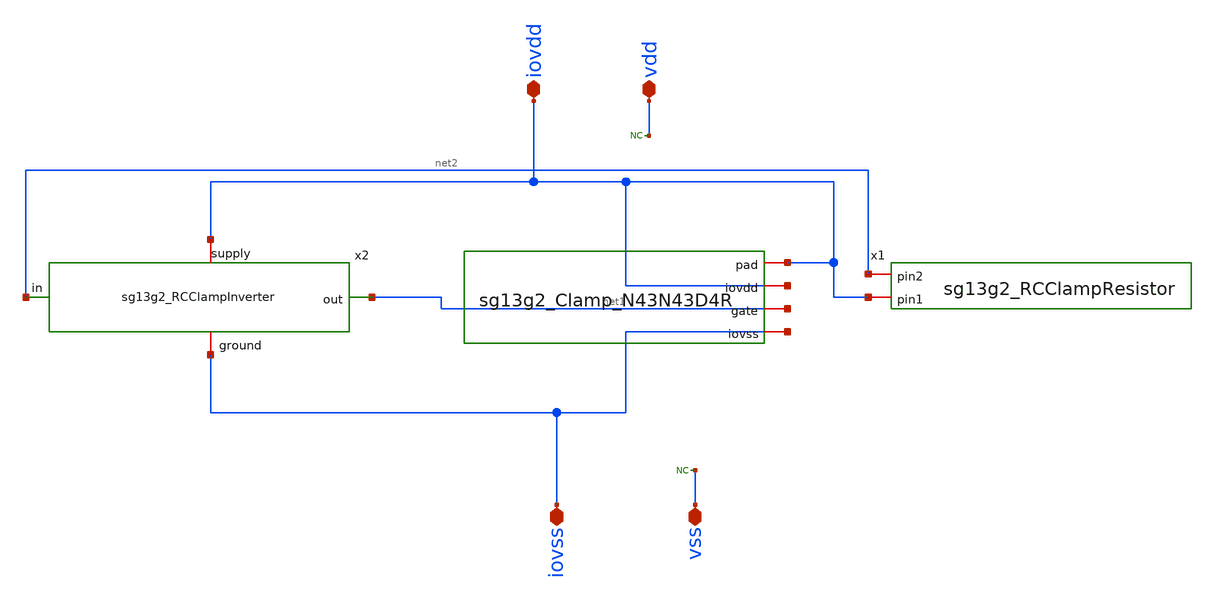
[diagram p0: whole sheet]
** sch_path: OTA_Telescopic_NO_FLATTEN/Schematics_and_Symbols/IOCells/sg13g2_IOPadIOVdd.sch
**.subckt sg13g2_IOPadIOVdd iovss iovdd vss vdd
*.iopin iovss
*.iopin iovdd
*.iopin vss
*.iopin vdd
x1 iovdd iovdd net1 iovss sg13g2_Clamp_N43N43D4R
x1 net2 iovdd sg13g2_RCClampResistor
x2 iovdd net1 net2 iovss sg13g2_RCClampInverter
* noconn vss
* noconn vdd
**.ends

* expanding   symbol:  sg13g2_Clamp_N43N43D4R.sym # of pins=4
** sym_path: OTA_Telescopic_v3/Schematics_and_Symbols/IOCells/sg13g2_Clamp_N43N43D4R.sym
** sch_path: OTA_Telescopic_v3/Schematics_and_Symbols/IOCells/sg13g2_Clamp_N43N43D4R.sch
.subckt sg13g2_Clamp_N43N43D4R pad iovdd gate iovss
*.iopin pad
*.iopin iovss
*.iopin gate
*.iopin iovdd
XM1 iovss gate pad iovss sg13_hv_nmos w=4.4u l=0.6u ng=1 m=1 mm_ok=1
XM2 iovss gate pad iovss sg13_hv_nmos w=4.4u l=0.6u ng=1 m=1 mm_ok=1
XM3 iovss gate pad iovss sg13_hv_nmos w=4.4u l=0.6u ng=1 m=1 mm_ok=1
XM4 iovss gate pad iovss sg13_hv_nmos w=4.4u l=0.6u ng=1 m=1 mm_ok=1
XM5 iovss gate pad iovss sg13_hv_nmos w=4.4u l=0.6u ng=1 m=1 mm_ok=1
XM6 iovss gate pad iovss sg13_hv_nmos w=4.4u l=0.6u ng=1 m=1 mm_ok=1
XM7 iovss gate pad iovss sg13_hv_nmos w=4.4u l=0.6u ng=1 m=1 mm_ok=1
XM8 iovss gate pad iovss sg13_hv_nmos w=4.4u l=0.6u ng=1 m=1 mm_ok=1
XM9 iovss gate pad iovss sg13_hv_nmos w=4.4u l=0.6u ng=1 m=1 mm_ok=1
XM10 iovss gate pad iovss sg13_hv_nmos w=4.4u l=0.6u ng=1 m=1 mm_ok=1
XM11 iovss gate pad iovss sg13_hv_nmos w=4.4u l=0.6u ng=1 m=1 mm_ok=1
XM12 iovss gate pad iovss sg13_hv_nmos w=4.4u l=0.6u ng=1 m=1 mm_ok=1
XM13 iovss gate pad iovss sg13_hv_nmos w=4.4u l=0.6u ng=1 m=1 mm_ok=1
XM14 iovss gate pad iovss sg13_hv_nmos w=4.4u l=0.6u ng=1 m=1 mm_ok=1
XM15 iovss gate pad iovss sg13_hv_nmos w=4.4u l=0.6u ng=1 m=1 mm_ok=1
XM16 iovss gate pad iovss sg13_hv_nmos w=4.4u l=0.6u ng=1 m=1 mm_ok=1
XM17 iovss gate pad iovss sg13_hv_nmos w=4.4u l=0.6u ng=1 m=1 mm_ok=1
XM18 iovss gate pad iovss sg13_hv_nmos w=4.4u l=0.6u ng=1 m=1 mm_ok=1
XM19 iovss gate pad iovss sg13_hv_nmos w=4.4u l=0.6u ng=1 m=1 mm_ok=1
XM20 iovss gate pad iovss sg13_hv_nmos w=4.4u l=0.6u ng=1 m=1 mm_ok=1
XM21 iovss gate pad iovss sg13_hv_nmos w=4.4u l=0.6u ng=1 m=1 mm_ok=1
XM22 iovss gate pad iovss sg13_hv_nmos w=4.4u l=0.6u ng=1 m=1 mm_ok=1
XM23 iovss gate pad iovss sg13_hv_nmos w=4.4u l=0.6u ng=1 m=1 mm_ok=1
XM24 iovss gate pad iovss sg13_hv_nmos w=4.4u l=0.6u ng=1 m=1 mm_ok=1
XM25 iovss gate pad iovss sg13_hv_nmos w=4.4u l=0.6u ng=1 m=1 mm_ok=1
XM26 iovss gate pad iovss sg13_hv_nmos w=4.4u l=0.6u ng=1 m=1 mm_ok=1
XM27 iovss gate pad iovss sg13_hv_nmos w=4.4u l=0.6u ng=1 m=1 mm_ok=1
XM28 iovss gate pad iovss sg13_hv_nmos w=4.4u l=0.6u ng=1 m=1 mm_ok=1
XM29 iovss gate pad iovss sg13_hv_nmos w=4.4u l=0.6u ng=1 m=1 mm_ok=1
XM30 iovss gate pad iovss sg13_hv_nmos w=4.4u l=0.6u ng=1 m=1 mm_ok=1
XM31 iovss gate pad iovss sg13_hv_nmos w=4.4u l=0.6u ng=1 m=1 mm_ok=1
XM32 iovss gate pad iovss sg13_hv_nmos w=4.4u l=0.6u ng=1 m=1 mm_ok=1
XM33 iovss gate pad iovss sg13_hv_nmos w=4.4u l=0.6u ng=1 m=1 mm_ok=1
XM34 iovss gate pad iovss sg13_hv_nmos w=4.4u l=0.6u ng=1 m=1 mm_ok=1
XM35 iovss gate pad iovss sg13_hv_nmos w=4.4u l=0.6u ng=1 m=1 mm_ok=1
XM36 iovss gate pad iovss sg13_hv_nmos w=4.4u l=0.6u ng=1 m=1 mm_ok=1
XM37 iovss gate pad iovss sg13_hv_nmos w=4.4u l=0.6u ng=1 m=1 mm_ok=1
XM38 iovss gate pad iovss sg13_hv_nmos w=4.4u l=0.6u ng=1 m=1 mm_ok=1
XM39 iovss gate pad iovss sg13_hv_nmos w=4.4u l=0.6u ng=1 m=1 mm_ok=1
XM40 iovss gate pad iovss sg13_hv_nmos w=4.4u l=0.6u ng=1 m=1 mm_ok=1
XM41 iovss gate pad iovss sg13_hv_nmos w=4.4u l=0.6u ng=1 m=1 mm_ok=1
XM42 iovss gate pad iovss sg13_hv_nmos w=4.4u l=0.6u ng=1 m=1 mm_ok=1
XM43 iovss gate pad iovss sg13_hv_nmos w=4.4u l=0.6u ng=1 m=1 mm_ok=1
XM44 iovss gate pad iovss sg13_hv_nmos w=4.4u l=0.6u ng=1 m=1 mm_ok=1
XM45 iovss gate pad iovss sg13_hv_nmos w=4.4u l=0.6u ng=1 m=1 mm_ok=1
XM46 iovss gate pad iovss sg13_hv_nmos w=4.4u l=0.6u ng=1 m=1 mm_ok=1
XM47 iovss gate pad iovss sg13_hv_nmos w=4.4u l=0.6u ng=1 m=1 mm_ok=1
XM48 iovss gate pad iovss sg13_hv_nmos w=4.4u l=0.6u ng=1 m=1 mm_ok=1
XM49 iovss gate pad iovss sg13_hv_nmos w=4.4u l=0.6u ng=1 m=1 mm_ok=1
XM50 iovss gate pad iovss sg13_hv_nmos w=4.4u l=0.6u ng=1 m=1 mm_ok=1
XM51 iovss gate pad iovss sg13_hv_nmos w=4.4u l=0.6u ng=1 m=1 mm_ok=1
XM52 iovss gate pad iovss sg13_hv_nmos w=4.4u l=0.6u ng=1 m=1 mm_ok=1
XM53 iovss gate pad iovss sg13_hv_nmos w=4.4u l=0.6u ng=1 m=1 mm_ok=1
XM54 iovss gate pad iovss sg13_hv_nmos w=4.4u l=0.6u ng=1 m=1 mm_ok=1
XM55 iovss gate pad iovss sg13_hv_nmos w=4.4u l=0.6u ng=1 m=1 mm_ok=1
XM56 iovss gate pad iovss sg13_hv_nmos w=4.4u l=0.6u ng=1 m=1 mm_ok=1
XM57 iovss gate pad iovss sg13_hv_nmos w=4.4u l=0.6u ng=1 m=1 mm_ok=1
XM58 iovss gate pad iovss sg13_hv_nmos w=4.4u l=0.6u ng=1 m=1 mm_ok=1
XM59 iovss gate pad iovss sg13_hv_nmos w=4.4u l=0.6u ng=1 m=1 mm_ok=1
XM60 iovss gate pad iovss sg13_hv_nmos w=4.4u l=0.6u ng=1 m=1 mm_ok=1
XM61 iovss gate pad iovss sg13_hv_nmos w=4.4u l=0.6u ng=1 m=1 mm_ok=1
XM62 iovss gate pad iovss sg13_hv_nmos w=4.4u l=0.6u ng=1 m=1 mm_ok=1
XM63 iovss gate pad iovss sg13_hv_nmos w=4.4u l=0.6u ng=1 m=1 mm_ok=1
XM64 iovss gate pad iovss sg13_hv_nmos w=4.4u l=0.6u ng=1 m=1 mm_ok=1
XM65 iovss gate pad iovss sg13_hv_nmos w=4.4u l=0.6u ng=1 m=1 mm_ok=1
XM66 iovss gate pad iovss sg13_hv_nmos w=4.4u l=0.6u ng=1 m=1 mm_ok=1
XM67 iovss gate pad iovss sg13_hv_nmos w=4.4u l=0.6u ng=1 m=1 mm_ok=1
XM68 iovss gate pad iovss sg13_hv_nmos w=4.4u l=0.6u ng=1 m=1 mm_ok=1
XM69 iovss gate pad iovss sg13_hv_nmos w=4.4u l=0.6u ng=1 m=1 mm_ok=1
XM70 iovss gate pad iovss sg13_hv_nmos w=4.4u l=0.6u ng=1 m=1 mm_ok=1
XM71 iovss gate pad iovss sg13_hv_nmos w=4.4u l=0.6u ng=1 m=1 mm_ok=1
XM72 iovss gate pad iovss sg13_hv_nmos w=4.4u l=0.6u ng=1 m=1 mm_ok=1
XM73 iovss gate pad iovss sg13_hv_nmos w=4.4u l=0.6u ng=1 m=1 mm_ok=1
XM74 iovss gate pad iovss sg13_hv_nmos w=4.4u l=0.6u ng=1 m=1 mm_ok=1
XM75 iovss gate pad iovss sg13_hv_nmos w=4.4u l=0.6u ng=1 m=1 mm_ok=1
XM76 iovss gate pad iovss sg13_hv_nmos w=4.4u l=0.6u ng=1 m=1 mm_ok=1
XM77 iovss gate pad iovss sg13_hv_nmos w=4.4u l=0.6u ng=1 m=1 mm_ok=1
XM78 iovss gate pad iovss sg13_hv_nmos w=4.4u l=0.6u ng=1 m=1 mm_ok=1
XM79 iovss gate pad iovss sg13_hv_nmos w=4.4u l=0.6u ng=1 m=1 mm_ok=1
XM80 iovss gate pad iovss sg13_hv_nmos w=4.4u l=0.6u ng=1 m=1 mm_ok=1
XM81 iovss gate pad iovss sg13_hv_nmos w=4.4u l=0.6u ng=1 m=1 mm_ok=1
XM82 iovss gate pad iovss sg13_hv_nmos w=4.4u l=0.6u ng=1 m=1 mm_ok=1
XM83 iovss gate pad iovss sg13_hv_nmos w=4.4u l=0.6u ng=1 m=1 mm_ok=1
XM84 iovss gate pad iovss sg13_hv_nmos w=4.4u l=0.6u ng=1 m=1 mm_ok=1
XM85 iovss gate pad iovss sg13_hv_nmos w=4.4u l=0.6u ng=1 m=1 mm_ok=1
XM86 iovss gate pad iovss sg13_hv_nmos w=4.4u l=0.6u ng=1 m=1 mm_ok=1
XM87 iovss gate pad iovss sg13_hv_nmos w=4.4u l=0.6u ng=1 m=1 mm_ok=1
XM88 iovss gate pad iovss sg13_hv_nmos w=4.4u l=0.6u ng=1 m=1 mm_ok=1
XM89 iovss gate pad iovss sg13_hv_nmos w=4.4u l=0.6u ng=1 m=1 mm_ok=1
XM90 iovss gate pad iovss sg13_hv_nmos w=4.4u l=0.6u ng=1 m=1 mm_ok=1
XM91 iovss gate pad iovss sg13_hv_nmos w=4.4u l=0.6u ng=1 m=1 mm_ok=1
XM92 iovss gate pad iovss sg13_hv_nmos w=4.4u l=0.6u ng=1 m=1 mm_ok=1
XM93 iovss gate pad iovss sg13_hv_nmos w=4.4u l=0.6u ng=1 m=1 mm_ok=1
XM94 iovss gate pad iovss sg13_hv_nmos w=4.4u l=0.6u ng=1 m=1 mm_ok=1
XM95 iovss gate pad iovss sg13_hv_nmos w=4.4u l=0.6u ng=1 m=1 mm_ok=1
XM96 iovss gate pad iovss sg13_hv_nmos w=4.4u l=0.6u ng=1 m=1 mm_ok=1
XM97 iovss gate pad iovss sg13_hv_nmos w=4.4u l=0.6u ng=1 m=1 mm_ok=1
XM98 iovss gate pad iovss sg13_hv_nmos w=4.4u l=0.6u ng=1 m=1 mm_ok=1
XM99 iovss gate pad iovss sg13_hv_nmos w=4.4u l=0.6u ng=1 m=1 mm_ok=1
XM100 iovss gate pad iovss sg13_hv_nmos w=4.4u l=0.6u ng=1 m=1 mm_ok=1
XM101 iovss gate pad iovss sg13_hv_nmos w=4.4u l=0.6u ng=1 m=1 mm_ok=1
XM102 iovss gate pad iovss sg13_hv_nmos w=4.4u l=0.6u ng=1 m=1 mm_ok=1
XM103 iovss gate pad iovss sg13_hv_nmos w=4.4u l=0.6u ng=1 m=1 mm_ok=1
XM104 iovss gate pad iovss sg13_hv_nmos w=4.4u l=0.6u ng=1 m=1 mm_ok=1
XM105 iovss gate pad iovss sg13_hv_nmos w=4.4u l=0.6u ng=1 m=1 mm_ok=1
XM106 iovss gate pad iovss sg13_hv_nmos w=4.4u l=0.6u ng=1 m=1 mm_ok=1
XM107 iovss gate pad iovss sg13_hv_nmos w=4.4u l=0.6u ng=1 m=1 mm_ok=1
XM108 iovss gate pad iovss sg13_hv_nmos w=4.4u l=0.6u ng=1 m=1 mm_ok=1
XM109 iovss gate pad iovss sg13_hv_nmos w=4.4u l=0.6u ng=1 m=1 mm_ok=1
XM110 iovss gate pad iovss sg13_hv_nmos w=4.4u l=0.6u ng=1 m=1 mm_ok=1
XM111 iovss gate pad iovss sg13_hv_nmos w=4.4u l=0.6u ng=1 m=1 mm_ok=1
XM112 iovss gate pad iovss sg13_hv_nmos w=4.4u l=0.6u ng=1 m=1 mm_ok=1
XM113 iovss gate pad iovss sg13_hv_nmos w=4.4u l=0.6u ng=1 m=1 mm_ok=1
XM114 iovss gate pad iovss sg13_hv_nmos w=4.4u l=0.6u ng=1 m=1 mm_ok=1
XM115 iovss gate pad iovss sg13_hv_nmos w=4.4u l=0.6u ng=1 m=1 mm_ok=1
XM116 iovss gate pad iovss sg13_hv_nmos w=4.4u l=0.6u ng=1 m=1 mm_ok=1
XM117 iovss gate pad iovss sg13_hv_nmos w=4.4u l=0.6u ng=1 m=1 mm_ok=1
XM118 iovss gate pad iovss sg13_hv_nmos w=4.4u l=0.6u ng=1 m=1 mm_ok=1
XM119 iovss gate pad iovss sg13_hv_nmos w=4.4u l=0.6u ng=1 m=1 mm_ok=1
XM120 iovss gate pad iovss sg13_hv_nmos w=4.4u l=0.6u ng=1 m=1 mm_ok=1
XM121 iovss gate pad iovss sg13_hv_nmos w=4.4u l=0.6u ng=1 m=1 mm_ok=1
XM122 iovss gate pad iovss sg13_hv_nmos w=4.4u l=0.6u ng=1 m=1 mm_ok=1
XM123 iovss gate pad iovss sg13_hv_nmos w=4.4u l=0.6u ng=1 m=1 mm_ok=1
XM124 iovss gate pad iovss sg13_hv_nmos w=4.4u l=0.6u ng=1 m=1 mm_ok=1
XM125 iovss gate pad iovss sg13_hv_nmos w=4.4u l=0.6u ng=1 m=1 mm_ok=1
XM126 iovss gate pad iovss sg13_hv_nmos w=4.4u l=0.6u ng=1 m=1 mm_ok=1
XM127 iovss gate pad iovss sg13_hv_nmos w=4.4u l=0.6u ng=1 m=1 mm_ok=1
XM128 iovss gate pad iovss sg13_hv_nmos w=4.4u l=0.6u ng=1 m=1 mm_ok=1
XM129 iovss gate pad iovss sg13_hv_nmos w=4.4u l=0.6u ng=1 m=1 mm_ok=1
XM130 iovss gate pad iovss sg13_hv_nmos w=4.4u l=0.6u ng=1 m=1 mm_ok=1
XM131 iovss gate pad iovss sg13_hv_nmos w=4.4u l=0.6u ng=1 m=1 mm_ok=1
XM132 iovss gate pad iovss sg13_hv_nmos w=4.4u l=0.6u ng=1 m=1 mm_ok=1
XM133 iovss gate pad iovss sg13_hv_nmos w=4.4u l=0.6u ng=1 m=1 mm_ok=1
XM134 iovss gate pad iovss sg13_hv_nmos w=4.4u l=0.6u ng=1 m=1 mm_ok=1
XM135 iovss gate pad iovss sg13_hv_nmos w=4.4u l=0.6u ng=1 m=1 mm_ok=1
XM136 iovss gate pad iovss sg13_hv_nmos w=4.4u l=0.6u ng=1 m=1 mm_ok=1
XM137 iovss gate pad iovss sg13_hv_nmos w=4.4u l=0.6u ng=1 m=1 mm_ok=1
XM138 iovss gate pad iovss sg13_hv_nmos w=4.4u l=0.6u ng=1 m=1 mm_ok=1
XM139 iovss gate pad iovss sg13_hv_nmos w=4.4u l=0.6u ng=1 m=1 mm_ok=1
XM140 iovss gate pad iovss sg13_hv_nmos w=4.4u l=0.6u ng=1 m=1 mm_ok=1
XM141 iovss gate pad iovss sg13_hv_nmos w=4.4u l=0.6u ng=1 m=1 mm_ok=1
XM142 iovss gate pad iovss sg13_hv_nmos w=4.4u l=0.6u ng=1 m=1 mm_ok=1
XM143 iovss gate pad iovss sg13_hv_nmos w=4.4u l=0.6u ng=1 m=1 mm_ok=1
XM144 iovss gate pad iovss sg13_hv_nmos w=4.4u l=0.6u ng=1 m=1 mm_ok=1
XM145 iovss gate pad iovss sg13_hv_nmos w=4.4u l=0.6u ng=1 m=1 mm_ok=1
XM146 iovss gate pad iovss sg13_hv_nmos w=4.4u l=0.6u ng=1 m=1 mm_ok=1
XM147 iovss gate pad iovss sg13_hv_nmos w=4.4u l=0.6u ng=1 m=1 mm_ok=1
XM148 iovss gate pad iovss sg13_hv_nmos w=4.4u l=0.6u ng=1 m=1 mm_ok=1
XM149 iovss gate pad iovss sg13_hv_nmos w=4.4u l=0.6u ng=1 m=1 mm_ok=1
XM150 iovss gate pad iovss sg13_hv_nmos w=4.4u l=0.6u ng=1 m=1 mm_ok=1
XM151 iovss gate pad iovss sg13_hv_nmos w=4.4u l=0.6u ng=1 m=1 mm_ok=1
XM152 iovss gate pad iovss sg13_hv_nmos w=4.4u l=0.6u ng=1 m=1 mm_ok=1
XM153 iovss gate pad iovss sg13_hv_nmos w=4.4u l=0.6u ng=1 m=1 mm_ok=1
XM154 iovss gate pad iovss sg13_hv_nmos w=4.4u l=0.6u ng=1 m=1 mm_ok=1
XM155 iovss gate pad iovss sg13_hv_nmos w=4.4u l=0.6u ng=1 m=1 mm_ok=1
XM156 iovss gate pad iovss sg13_hv_nmos w=4.4u l=0.6u ng=1 m=1 mm_ok=1
XM157 iovss gate pad iovss sg13_hv_nmos w=4.4u l=0.6u ng=1 m=1 mm_ok=1
XM158 iovss gate pad iovss sg13_hv_nmos w=4.4u l=0.6u ng=1 m=1 mm_ok=1
XM159 iovss gate pad iovss sg13_hv_nmos w=4.4u l=0.6u ng=1 m=1 mm_ok=1
XM160 iovss gate pad iovss sg13_hv_nmos w=4.4u l=0.6u ng=1 m=1 mm_ok=1
XM161 iovss gate pad iovss sg13_hv_nmos w=4.4u l=0.6u ng=1 m=1 mm_ok=1
XM162 iovss gate pad iovss sg13_hv_nmos w=4.4u l=0.6u ng=1 m=1 mm_ok=1
XM163 iovss gate pad iovss sg13_hv_nmos w=4.4u l=0.6u ng=1 m=1 mm_ok=1
XM164 iovss gate pad iovss sg13_hv_nmos w=4.4u l=0.6u ng=1 m=1 mm_ok=1
XM165 iovss gate pad iovss sg13_hv_nmos w=4.4u l=0.6u ng=1 m=1 mm_ok=1
XM166 iovss gate pad iovss sg13_hv_nmos w=4.4u l=0.6u ng=1 m=1 mm_ok=1
XM167 iovss gate pad iovss sg13_hv_nmos w=4.4u l=0.6u ng=1 m=1 mm_ok=1
XM168 iovss gate pad iovss sg13_hv_nmos w=4.4u l=0.6u ng=1 m=1 mm_ok=1
XM169 iovss gate pad iovss sg13_hv_nmos w=4.4u l=0.6u ng=1 m=1 mm_ok=1
XM170 iovss gate pad iovss sg13_hv_nmos w=4.4u l=0.6u ng=1 m=1 mm_ok=1
XM171 iovss gate pad iovss sg13_hv_nmos w=4.4u l=0.6u ng=1 m=1 mm_ok=1
XM172 iovss gate pad iovss sg13_hv_nmos w=4.4u l=0.6u ng=1 m=1 mm_ok=1
XD1 iovss gate dantenna l=0.64u w=0.48u
* noconn iovdd
.ends


* expanding   symbol:  sg13g2_RCClampResistor.sym # of pins=2
** sym_path: sg13g2_RCClampResistor.sym
** sch_path: sg13g2_RCClampResistor.sch
.subckt sg13g2_RCClampResistor pin2 pin1
*.iopin pin1
*.iopin pin2
XR1 net1 pin1 sub! rppd w=1.0e-6 l=20.0e-6 m=1 b=0 mm_ok=1
XR2 net2 net1 sub! rppd w=1.0e-6 l=20.0e-6 m=1 b=0 mm_ok=1
XR3 net3 net2 sub! rppd w=1.0e-6 l=20.0e-6 m=1 b=0 mm_ok=1
XR4 net4 net3 sub! rppd w=1.0e-6 l=20.0e-6 m=1 b=0 mm_ok=1
XR5 net7 net8 sub! rppd w=1.0e-6 l=20.0e-6 m=1 b=0 mm_ok=1
XR6 net6 net7 sub! rppd w=1.0e-6 l=20.0e-6 m=1 b=0 mm_ok=1
XR7 net5 net6 sub! rppd w=1.0e-6 l=20.0e-6 m=1 b=0 mm_ok=1
XR8 net4 net5 sub! rppd w=1.0e-6 l=20.0e-6 m=1 b=0 mm_ok=1
XR9 net9 net8 sub! rppd w=1.0e-6 l=20.0e-6 m=1 b=0 mm_ok=1
XR10 net10 net9 sub! rppd w=1.0e-6 l=20.0e-6 m=1 b=0 mm_ok=1
XR11 net11 net10 sub! rppd w=1.0e-6 l=20.0e-6 m=1 b=0 mm_ok=1
XR12 net12 net11 sub! rppd w=1.0e-6 l=20.0e-6 m=1 b=0 mm_ok=1
XR13 net15 net16 sub! rppd w=1.0e-6 l=20.0e-6 m=1 b=0 mm_ok=1
XR14 net14 net15 sub! rppd w=1.0e-6 l=20.0e-6 m=1 b=0 mm_ok=1
XR15 net13 net14 sub! rppd w=1.0e-6 l=20.0e-6 m=1 b=0 mm_ok=1
XR16 net12 net13 sub! rppd w=1.0e-6 l=20.0e-6 m=1 b=0 mm_ok=1
XR17 net17 net16 sub! rppd w=1.0e-6 l=20.0e-6 m=1 b=0 mm_ok=1
XR18 net18 net17 sub! rppd w=1.0e-6 l=20.0e-6 m=1 b=0 mm_ok=1
XR19 net19 net18 sub! rppd w=1.0e-6 l=20.0e-6 m=1 b=0 mm_ok=1
XR20 net20 net19 sub! rppd w=1.0e-6 l=20.0e-6 m=1 b=0 mm_ok=1
XR21 net23 net24 sub! rppd w=1.0e-6 l=20.0e-6 m=1 b=0 mm_ok=1
XR22 net22 net23 sub! rppd w=1.0e-6 l=20.0e-6 m=1 b=0 mm_ok=1
XR23 net21 net22 sub! rppd w=1.0e-6 l=20.0e-6 m=1 b=0 mm_ok=1
XR24 net20 net21 sub! rppd w=1.0e-6 l=20.0e-6 m=1 b=0 mm_ok=1
XR25 net25 net24 sub! rppd w=1.0e-6 l=20.0e-6 m=1 b=0 mm_ok=1
XR26 pin2 net25 sub! rppd w=1.0e-6 l=20.0e-6 m=1 b=0 mm_ok=1
.ends


* expanding   symbol:  sg13g2_RCClampInverter.sym # of pins=4
** sym_path: sg13g2_RCClampInverter.sym
** sch_path: sg13g2_RCClampInverter.sch
.subckt sg13g2_RCClampInverter supply out in ground
*.iopin supply
*.iopin ground
*.opin out
*.ipin in
XM1 ground in ground ground sg13_hv_nmos w=9.0u l=9.5u ng=1 m=1 mm_ok=1
XM2 ground in ground ground sg13_hv_nmos w=9.0u l=9.5u ng=1 m=1 mm_ok=1
XM3 ground in ground ground sg13_hv_nmos w=9.0u l=9.5u ng=1 m=1 mm_ok=1
XM4 ground in ground ground sg13_hv_nmos w=9.0u l=9.5u ng=1 m=1 mm_ok=1
XM5 ground in ground ground sg13_hv_nmos w=9.0u l=9.5u ng=1 m=1 mm_ok=1
XM6 ground in ground ground sg13_hv_nmos w=9.0u l=9.5u ng=1 m=1 mm_ok=1
XM7 ground in ground ground sg13_hv_nmos w=9.0u l=9.5u ng=1 m=1 mm_ok=1
XM8 ground in ground ground sg13_hv_nmos w=9.0u l=9.5u ng=1 m=1 mm_ok=1
XM9 ground in ground ground sg13_hv_nmos w=9.0u l=9.5u ng=1 m=1 mm_ok=1
XM10 ground in ground ground sg13_hv_nmos w=9.0u l=9.5u ng=1 m=1 mm_ok=1
XM11 ground in ground ground sg13_hv_nmos w=9.0u l=9.5u ng=1 m=1 mm_ok=1
XM12 ground in ground ground sg13_hv_nmos w=9.0u l=9.5u ng=1 m=1 mm_ok=1
XM13 ground in ground ground sg13_hv_nmos w=9.0u l=9.5u ng=1 m=1 mm_ok=1
XM14 ground in ground ground sg13_hv_nmos w=9.0u l=9.5u ng=1 m=1 mm_ok=1
XM15 out in ground ground sg13_hv_nmos w=9.0u l=0.5u ng=1 m=1 mm_ok=1
XM16 out in ground ground sg13_hv_nmos w=9.0u l=0.5u ng=1 m=1 mm_ok=1
XM17 out in ground ground sg13_hv_nmos w=9.0u l=0.5u ng=1 m=1 mm_ok=1
XM18 out in ground ground sg13_hv_nmos w=9.0u l=0.5u ng=1 m=1 mm_ok=1
XM19 out in ground ground sg13_hv_nmos w=9.0u l=0.5u ng=1 m=1 mm_ok=1
XM20 out in ground ground sg13_hv_nmos w=9.0u l=0.5u ng=1 m=1 mm_ok=1
XM21 out in ground ground sg13_hv_nmos w=9.0u l=0.5u ng=1 m=1 mm_ok=1
XM22 out in ground ground sg13_hv_nmos w=9.0u l=0.5u ng=1 m=1 mm_ok=1
XM23 out in ground ground sg13_hv_nmos w=9.0u l=0.5u ng=1 m=1 mm_ok=1
XM24 out in ground ground sg13_hv_nmos w=9.0u l=0.5u ng=1 m=1 mm_ok=1
XM25 out in ground ground sg13_hv_nmos w=9.0u l=0.5u ng=1 m=1 mm_ok=1
XM26 out in ground ground sg13_hv_nmos w=9.0u l=0.5u ng=1 m=1 mm_ok=1
XM27 out in supply supply sg13_hv_pmos w=7.0u l=0.5u ng=1 m=1 mm_ok=1
XM28 out in supply supply sg13_hv_pmos w=7.0u l=0.5u ng=1 m=1 mm_ok=1
XM29 out in supply supply sg13_hv_pmos w=7.0u l=0.5u ng=1 m=1 mm_ok=1
XM30 out in supply supply sg13_hv_pmos w=7.0u l=0.5u ng=1 m=1 mm_ok=1
XM31 out in supply supply sg13_hv_pmos w=7.0u l=0.5u ng=1 m=1 mm_ok=1
XM32 out in supply supply sg13_hv_pmos w=7.0u l=0.5u ng=1 m=1 mm_ok=1
XM33 out in supply supply sg13_hv_pmos w=7.0u l=0.5u ng=1 m=1 mm_ok=1
XM34 out in supply supply sg13_hv_pmos w=7.0u l=0.5u ng=1 m=1 mm_ok=1
XM35 out in supply supply sg13_hv_pmos w=7.0u l=0.5u ng=1 m=1 mm_ok=1
XM36 out in supply supply sg13_hv_pmos w=7.0u l=0.5u ng=1 m=1 mm_ok=1
XM37 out in supply supply sg13_hv_pmos w=7.0u l=0.5u ng=1 m=1 mm_ok=1
XM38 out in supply supply sg13_hv_pmos w=7.0u l=0.5u ng=1 m=1 mm_ok=1
XM39 out in supply supply sg13_hv_pmos w=7.0u l=0.5u ng=1 m=1 mm_ok=1
XM40 out in supply supply sg13_hv_pmos w=7.0u l=0.5u ng=1 m=1 mm_ok=1
XM41 out in supply supply sg13_hv_pmos w=7.0u l=0.5u ng=1 m=1 mm_ok=1
XM42 out in supply supply sg13_hv_pmos w=7.0u l=0.5u ng=1 m=1 mm_ok=1
XM43 out in supply supply sg13_hv_pmos w=7.0u l=0.5u ng=1 m=1 mm_ok=1
XM44 out in supply supply sg13_hv_pmos w=7.0u l=0.5u ng=1 m=1 mm_ok=1
XM45 out in supply supply sg13_hv_pmos w=7.0u l=0.5u ng=1 m=1 mm_ok=1
XM46 out in supply supply sg13_hv_pmos w=7.0u l=0.5u ng=1 m=1 mm_ok=1
XM47 out in supply supply sg13_hv_pmos w=7.0u l=0.5u ng=1 m=1 mm_ok=1
XM48 out in supply supply sg13_hv_pmos w=7.0u l=0.5u ng=1 m=1 mm_ok=1
XM49 out in supply supply sg13_hv_pmos w=7.0u l=0.5u ng=1 m=1 mm_ok=1
XM50 out in supply supply sg13_hv_pmos w=7.0u l=0.5u ng=1 m=1 mm_ok=1
XM51 out in supply supply sg13_hv_pmos w=7.0u l=0.5u ng=1 m=1 mm_ok=1
XM52 out in supply supply sg13_hv_pmos w=7.0u l=0.5u ng=1 m=1 mm_ok=1
XM53 out in supply supply sg13_hv_pmos w=7.0u l=0.5u ng=1 m=1 mm_ok=1
XM54 out in supply supply sg13_hv_pmos w=7.0u l=0.5u ng=1 m=1 mm_ok=1
XM55 out in supply supply sg13_hv_pmos w=7.0u l=0.5u ng=1 m=1 mm_ok=1
XM56 out in supply supply sg13_hv_pmos w=7.0u l=0.5u ng=1 m=1 mm_ok=1
XM57 out in supply supply sg13_hv_pmos w=7.0u l=0.5u ng=1 m=1 mm_ok=1
XM58 out in supply supply sg13_hv_pmos w=7.0u l=0.5u ng=1 m=1 mm_ok=1
XM59 out in supply supply sg13_hv_pmos w=7.0u l=0.5u ng=1 m=1 mm_ok=1
XM60 out in supply supply sg13_hv_pmos w=7.0u l=0.5u ng=1 m=1 mm_ok=1
XM61 out in supply supply sg13_hv_pmos w=7.0u l=0.5u ng=1 m=1 mm_ok=1
XM62 out in supply supply sg13_hv_pmos w=7.0u l=0.5u ng=1 m=1 mm_ok=1
XM63 out in supply supply sg13_hv_pmos w=7.0u l=0.5u ng=1 m=1 mm_ok=1
XM64 out in supply supply sg13_hv_pmos w=7.0u l=0.5u ng=1 m=1 mm_ok=1
XM65 out in supply supply sg13_hv_pmos w=7.0u l=0.5u ng=1 m=1 mm_ok=1
XM66 out in supply supply sg13_hv_pmos w=7.0u l=0.5u ng=1 m=1 mm_ok=1
XM67 out in supply supply sg13_hv_pmos w=7.0u l=0.5u ng=1 m=1 mm_ok=1
XM68 out in supply supply sg13_hv_pmos w=7.0u l=0.5u ng=1 m=1 mm_ok=1
XM69 out in supply supply sg13_hv_pmos w=7.0u l=0.5u ng=1 m=1 mm_ok=1
XM70 out in supply supply sg13_hv_pmos w=7.0u l=0.5u ng=1 m=1 mm_ok=1
XM71 out in supply supply sg13_hv_pmos w=7.0u l=0.5u ng=1 m=1 mm_ok=1
XM72 out in supply supply sg13_hv_pmos w=7.0u l=0.5u ng=1 m=1 mm_ok=1
XM73 out in supply supply sg13_hv_pmos w=7.0u l=0.5u ng=1 m=1 mm_ok=1
XM74 out in supply supply sg13_hv_pmos w=7.0u l=0.5u ng=1 m=1 mm_ok=1
XM75 out in supply supply sg13_hv_pmos w=7.0u l=0.5u ng=1 m=1 mm_ok=1
XM76 out in supply supply sg13_hv_pmos w=7.0u l=0.5u ng=1 m=1 mm_ok=1
.ends

.end
